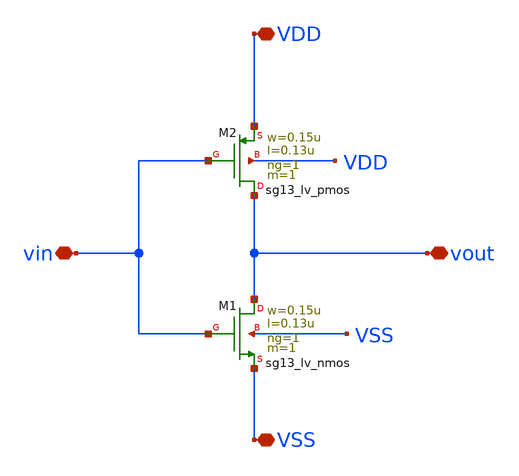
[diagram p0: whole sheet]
** sch_path: analog-db/templates/OTA-single-stage/inverter_stack.sch
**.subckt inverter_stack VDD VSS vout vin
*.iopin VDD
*.iopin VSS
*.iopin vout
*.iopin vin
XM1 vout vin VSS VSS sg13_lv_nmos w=0.15u l=0.13u ng=1 m=1 mm_ok=1
XM2 vout vin VDD VDD sg13_lv_pmos w=0.15u l=0.13u ng=1 m=1 mm_ok=1
**.ends
.end
